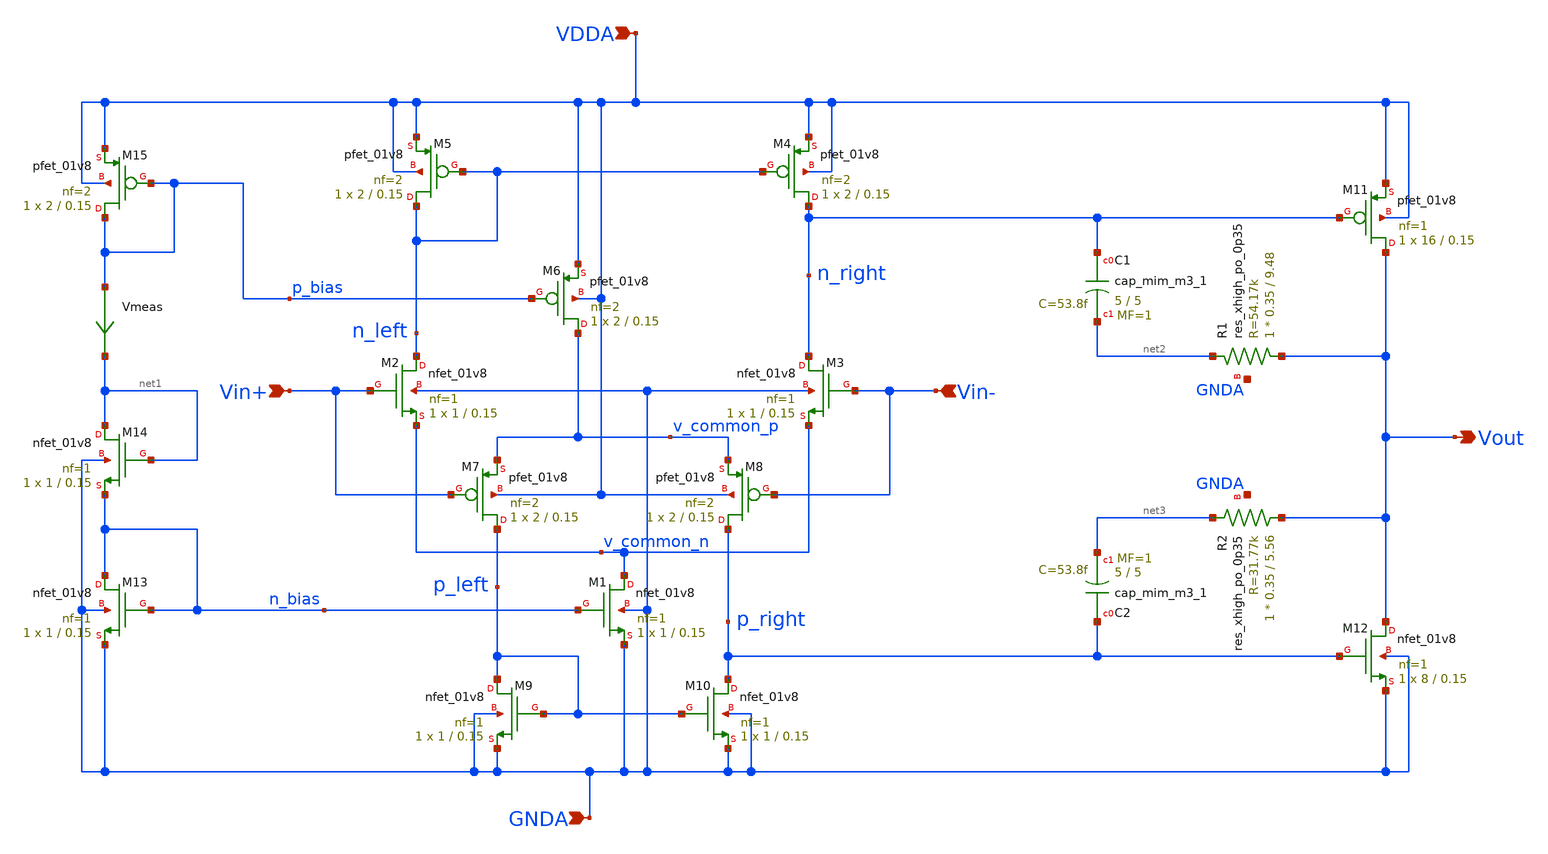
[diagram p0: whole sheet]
** sch_path: projects/pll/charge_pump/xschem_ngspice/rail_to_rail_opamp6.sch
**.subckt rail_to_rail_opamp6 Vout Vin+ Vin- VDDA GNDA
*.opin Vout
*.ipin Vin+
*.ipin Vin-
*.ipin VDDA
*.ipin GNDA
XM2 n_left Vin+ v_common_n GNDA sky130_fd_pr__nfet_01v8 L=0.15 W=1 nf=1 ad='int((nf+1)/2) * W/nf * 0.29'
+ as='int((nf+2)/2) * W/nf * 0.29' pd='2*int((nf+1)/2) * (W/nf + 0.29)' ps='2*int((nf+2)/2) * (W/nf + 0.29)'
+ nrd='0.29 / W' nrs='0.29 / W' sa=0 sb=0 sd=0 mult=1 m=1
XM3 n_right Vin- v_common_n GNDA sky130_fd_pr__nfet_01v8 L=0.15 W=1 nf=1 ad='int((nf+1)/2) * W/nf * 0.29'
+ as='int((nf+2)/2) * W/nf * 0.29' pd='2*int((nf+1)/2) * (W/nf + 0.29)' ps='2*int((nf+2)/2) * (W/nf + 0.29)'
+ nrd='0.29 / W' nrs='0.29 / W' sa=0 sb=0 sd=0 mult=1 m=1
XM5 n_left n_left VDDA VDDA sky130_fd_pr__pfet_01v8 L=0.15 W=2 nf=2 ad='int((nf+1)/2) * W/nf * 0.29'
+ as='int((nf+2)/2) * W/nf * 0.29' pd='2*int((nf+1)/2) * (W/nf + 0.29)' ps='2*int((nf+2)/2) * (W/nf + 0.29)'
+ nrd='0.29 / W' nrs='0.29 / W' sa=0 sb=0 sd=0 mult=1 m=1
XM4 n_right n_left VDDA VDDA sky130_fd_pr__pfet_01v8 L=0.15 W=2 nf=2 ad='int((nf+1)/2) * W/nf * 0.29'
+ as='int((nf+2)/2) * W/nf * 0.29' pd='2*int((nf+1)/2) * (W/nf + 0.29)' ps='2*int((nf+2)/2) * (W/nf + 0.29)'
+ nrd='0.29 / W' nrs='0.29 / W' sa=0 sb=0 sd=0 mult=1 m=1
XM6 v_common_p p_bias VDDA VDDA sky130_fd_pr__pfet_01v8 L=0.15 W=2 nf=2 ad='int((nf+1)/2) * W/nf * 0.29'
+ as='int((nf+2)/2) * W/nf * 0.29' pd='2*int((nf+1)/2) * (W/nf + 0.29)' ps='2*int((nf+2)/2) * (W/nf + 0.29)'
+ nrd='0.29 / W' nrs='0.29 / W' sa=0 sb=0 sd=0 mult=1 m=1
XM7 p_left Vin+ v_common_p VDDA sky130_fd_pr__pfet_01v8 L=0.15 W=2 nf=2 ad='int((nf+1)/2) * W/nf * 0.29'
+ as='int((nf+2)/2) * W/nf * 0.29' pd='2*int((nf+1)/2) * (W/nf + 0.29)' ps='2*int((nf+2)/2) * (W/nf + 0.29)'
+ nrd='0.29 / W' nrs='0.29 / W' sa=0 sb=0 sd=0 mult=1 m=1
XM8 p_right Vin- v_common_p VDDA sky130_fd_pr__pfet_01v8 L=0.15 W=2 nf=2 ad='int((nf+1)/2) * W/nf * 0.29'
+ as='int((nf+2)/2) * W/nf * 0.29' pd='2*int((nf+1)/2) * (W/nf + 0.29)' ps='2*int((nf+2)/2) * (W/nf + 0.29)'
+ nrd='0.29 / W' nrs='0.29 / W' sa=0 sb=0 sd=0 mult=1 m=1
XM9 p_left p_left GNDA GNDA sky130_fd_pr__nfet_01v8 L=0.15 W=1 nf=1 ad='int((nf+1)/2) * W/nf * 0.29'
+ as='int((nf+2)/2) * W/nf * 0.29' pd='2*int((nf+1)/2) * (W/nf + 0.29)' ps='2*int((nf+2)/2) * (W/nf + 0.29)'
+ nrd='0.29 / W' nrs='0.29 / W' sa=0 sb=0 sd=0 mult=1 m=1
XM10 p_right p_left GNDA GNDA sky130_fd_pr__nfet_01v8 L=0.15 W=1 nf=1 ad='int((nf+1)/2) * W/nf * 0.29'
+ as='int((nf+2)/2) * W/nf * 0.29' pd='2*int((nf+1)/2) * (W/nf + 0.29)' ps='2*int((nf+2)/2) * (W/nf + 0.29)'
+ nrd='0.29 / W' nrs='0.29 / W' sa=0 sb=0 sd=0 mult=1 m=1
XM1 v_common_n n_bias GNDA GNDA sky130_fd_pr__nfet_01v8 L=0.15 W=1 nf=1 ad='int((nf+1)/2) * W/nf * 0.29'
+ as='int((nf+2)/2) * W/nf * 0.29' pd='2*int((nf+1)/2) * (W/nf + 0.29)' ps='2*int((nf+2)/2) * (W/nf + 0.29)'
+ nrd='0.29 / W' nrs='0.29 / W' sa=0 sb=0 sd=0 mult=1 m=1
XM11 Vout n_right VDDA VDDA sky130_fd_pr__pfet_01v8 L=0.15 W=16 nf=1 ad='int((nf+1)/2) * W/nf * 0.29'
+ as='int((nf+2)/2) * W/nf * 0.29' pd='2*int((nf+1)/2) * (W/nf + 0.29)' ps='2*int((nf+2)/2) * (W/nf + 0.29)'
+ nrd='0.29 / W' nrs='0.29 / W' sa=0 sb=0 sd=0 mult=1 m=1
XM12 Vout p_right GNDA GNDA sky130_fd_pr__nfet_01v8 L=0.15 W=8 nf=1 ad='int((nf+1)/2) * W/nf * 0.29'
+ as='int((nf+2)/2) * W/nf * 0.29' pd='2*int((nf+1)/2) * (W/nf + 0.29)' ps='2*int((nf+2)/2) * (W/nf + 0.29)'
+ nrd='0.29 / W' nrs='0.29 / W' sa=0 sb=0 sd=0 mult=1 m=1
XM13 n_bias n_bias GNDA GNDA sky130_fd_pr__nfet_01v8 L=0.15 W=1 nf=1 ad='int((nf+1)/2) * W/nf * 0.29'
+ as='int((nf+2)/2) * W/nf * 0.29' pd='2*int((nf+1)/2) * (W/nf + 0.29)' ps='2*int((nf+2)/2) * (W/nf + 0.29)'
+ nrd='0.29 / W' nrs='0.29 / W' sa=0 sb=0 sd=0 mult=1 m=1
XM15 p_bias p_bias VDDA VDDA sky130_fd_pr__pfet_01v8 L=0.15 W=2 nf=2 ad='int((nf+1)/2) * W/nf * 0.29'
+ as='int((nf+2)/2) * W/nf * 0.29' pd='2*int((nf+1)/2) * (W/nf + 0.29)' ps='2*int((nf+2)/2) * (W/nf + 0.29)'
+ nrd='0.29 / W' nrs='0.29 / W' sa=0 sb=0 sd=0 mult=1 m=1
Vmeas p_bias net1 0
.save i(vmeas)
XM14 net1 net1 n_bias GNDA sky130_fd_pr__nfet_01v8 L=0.15 W=1 nf=1 ad='int((nf+1)/2) * W/nf * 0.29' as='int((nf+2)/2) * W/nf * 0.29'
+ pd='2*int((nf+1)/2) * (W/nf + 0.29)' ps='2*int((nf+2)/2) * (W/nf + 0.29)' nrd='0.29 / W' nrs='0.29 / W'
+ sa=0 sb=0 sd=0 mult=1 m=1
XC1 n_right net2 sky130_fd_pr__cap_mim_m3_1 W=5 L=5 MF=1 m=1
XC2 p_right net3 sky130_fd_pr__cap_mim_m3_1 W=5 L=5 MF=1 m=1
XR1 Vout net2 GNDA sky130_fd_pr__res_xhigh_po_0p35 L=9.48 mult=1 m=1
XR2 Vout net3 GNDA sky130_fd_pr__res_xhigh_po_0p35 L=5.56 mult=1 m=1
**.ends
.end
